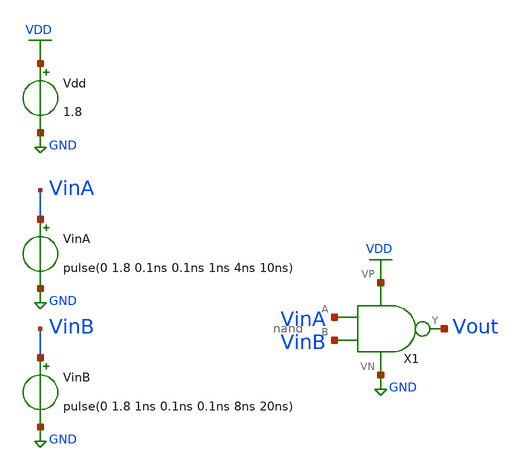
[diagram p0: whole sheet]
** sch_path: projects/nand/xschem_ngspice/nand_trans.sch
**.subckt nand_trans
X1 VinA VinB Vout VDD GND nand
Vdd VDD GND 1.8
VinA VinA GND pulse(0 1.8 0.1ns 0.1ns 1ns 4ns 10ns)
VinB VinB GND pulse(0 1.8 1ns 0.1ns 0.1ns 8ns 20ns)
**** begin user architecture code



.lib /foss/pdks/sky130A/libs.tech/ngspice/sky130.lib.spice tt

.tran 0.01n 1u

.save all



**** end user architecture code
**.ends

* expanding   symbol:  /foss/designs/my_design/projects/nand/xschem_ngspice/nand.sym # of pins=5
** sym_path: projects/nand/xschem_ngspice/nand.sym
** sch_path: projects/nand/xschem_ngspice/nand.sch
.subckt nand A B Y VP VN
*.ipin A
*.ipin B
*.opin Y
*.iopin VP
*.iopin VN
XM1 net1 A VN VN sky130_fd_pr__nfet_01v8 L=0.15 W=1 nf=1 ad='int((nf+1)/2) * W/nf * 0.29' as='int((nf+2)/2) * W/nf * 0.29'
+ pd='2*int((nf+1)/2) * (W/nf + 0.29)' ps='2*int((nf+2)/2) * (W/nf + 0.29)' nrd='0.29 / W' nrs='0.29 / W'
+ sa=0 sb=0 sd=0 mult=1 m=1
XM2 Y B net1 net1 sky130_fd_pr__nfet_01v8 L=0.15 W=1 nf=1 ad='int((nf+1)/2) * W/nf * 0.29' as='int((nf+2)/2) * W/nf * 0.29'
+ pd='2*int((nf+1)/2) * (W/nf + 0.29)' ps='2*int((nf+2)/2) * (W/nf + 0.29)' nrd='0.29 / W' nrs='0.29 / W'
+ sa=0 sb=0 sd=0 mult=1 m=1
XM3 Y B VP VP sky130_fd_pr__pfet_01v8 L=0.15 W=2 nf=1 ad='int((nf+1)/2) * W/nf * 0.29' as='int((nf+2)/2) * W/nf * 0.29'
+ pd='2*int((nf+1)/2) * (W/nf + 0.29)' ps='2*int((nf+2)/2) * (W/nf + 0.29)' nrd='0.29 / W' nrs='0.29 / W'
+ sa=0 sb=0 sd=0 mult=1 m=1
XM4 Y A VP VP sky130_fd_pr__pfet_01v8 L=0.15 W=2 nf=1 ad='int((nf+1)/2) * W/nf * 0.29' as='int((nf+2)/2) * W/nf * 0.29'
+ pd='2*int((nf+1)/2) * (W/nf + 0.29)' ps='2*int((nf+2)/2) * (W/nf + 0.29)' nrd='0.29 / W' nrs='0.29 / W'
+ sa=0 sb=0 sd=0 mult=1 m=1
.ends

.GLOBAL VDD
.GLOBAL GND
.end
